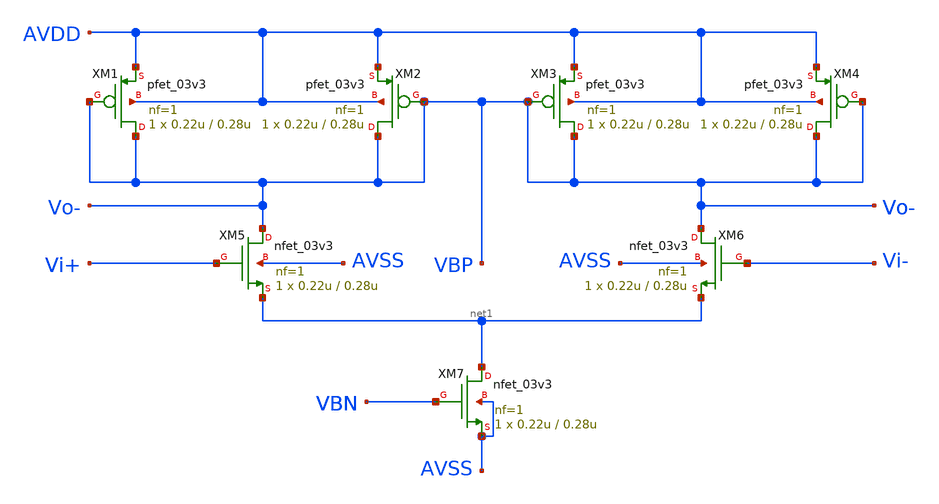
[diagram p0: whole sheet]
** sch_path: designs/untitled-1.sch
**.subckt untitled-1
XM1 VBP VBP AVDD AVDD pfet_03v3 L=0.28u W=0.22u nf=1 ad='int((nf+1)/2) * W/nf * 0.18u' as='int((nf+2)/2) * W/nf * 0.18u'
+ pd='2*int((nf+1)/2) * (W/nf + 0.18u)' ps='2*int((nf+2)/2) * (W/nf + 0.18u)' nrd='0.18u / W' nrs='0.18u / W'
+ sa=0 sb=0 sd=0 m=1
XM2 VBP VBP AVDD AVDD pfet_03v3 L=0.28u W=0.22u nf=1 ad='int((nf+1)/2) * W/nf * 0.18u' as='int((nf+2)/2) * W/nf * 0.18u'
+ pd='2*int((nf+1)/2) * (W/nf + 0.18u)' ps='2*int((nf+2)/2) * (W/nf + 0.18u)' nrd='0.18u / W' nrs='0.18u / W'
+ sa=0 sb=0 sd=0 m=1
XM3 VBP VBP AVDD AVDD pfet_03v3 L=0.28u W=0.22u nf=1 ad='int((nf+1)/2) * W/nf * 0.18u' as='int((nf+2)/2) * W/nf * 0.18u'
+ pd='2*int((nf+1)/2) * (W/nf + 0.18u)' ps='2*int((nf+2)/2) * (W/nf + 0.18u)' nrd='0.18u / W' nrs='0.18u / W'
+ sa=0 sb=0 sd=0 m=1
XM4 VBP VBP AVDD AVDD pfet_03v3 L=0.28u W=0.22u nf=1 ad='int((nf+1)/2) * W/nf * 0.18u' as='int((nf+2)/2) * W/nf * 0.18u'
+ pd='2*int((nf+1)/2) * (W/nf + 0.18u)' ps='2*int((nf+2)/2) * (W/nf + 0.18u)' nrd='0.18u / W' nrs='0.18u / W'
+ sa=0 sb=0 sd=0 m=1
XM5 VBP Vi+ net1 AVSS nfet_03v3 L=0.28u W=0.22u nf=1 ad='int((nf+1)/2) * W/nf * 0.18u' as='int((nf+2)/2) * W/nf * 0.18u'
+ pd='2*int((nf+1)/2) * (W/nf + 0.18u)' ps='2*int((nf+2)/2) * (W/nf + 0.18u)' nrd='0.18u / W' nrs='0.18u / W'
+ sa=0 sb=0 sd=0 m=1
XM6 VBP Vi- net1 AVSS nfet_03v3 L=0.28u W=0.22u nf=1 ad='int((nf+1)/2) * W/nf * 0.18u' as='int((nf+2)/2) * W/nf * 0.18u'
+ pd='2*int((nf+1)/2) * (W/nf + 0.18u)' ps='2*int((nf+2)/2) * (W/nf + 0.18u)' nrd='0.18u / W' nrs='0.18u / W'
+ sa=0 sb=0 sd=0 m=1
XM7 net1 VBN AVSS AVSS nfet_03v3 L=0.28u W=0.22u nf=1 ad='int((nf+1)/2) * W/nf * 0.18u' as='int((nf+2)/2) * W/nf * 0.18u'
+ pd='2*int((nf+1)/2) * (W/nf + 0.18u)' ps='2*int((nf+2)/2) * (W/nf + 0.18u)' nrd='0.18u / W' nrs='0.18u / W'
+ sa=0 sb=0 sd=0 m=1
**.ends
.end
